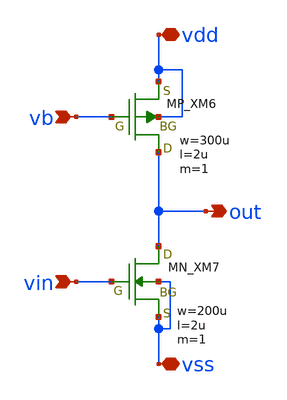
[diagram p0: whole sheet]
** sch_path: member_project/OPAMP/YutakaKOTANI/cs.sch
**.subckt cs vb vin out vss vdd
*.ipin vb
*.ipin vin
*.opin out
*.iopin vss
*.iopin vdd
XM6 out vb vdd vdd PMOS w=300u l=2u as=0 ad=0 ps=0 pd=0 nrd=0 nrs=0 m=1
XM7 out vin vss vss NMOS w=200u l=2u as=0 ad=0 ps=0 pd=0 nrd=0 nrs=0 m=1
**.ends
.end
